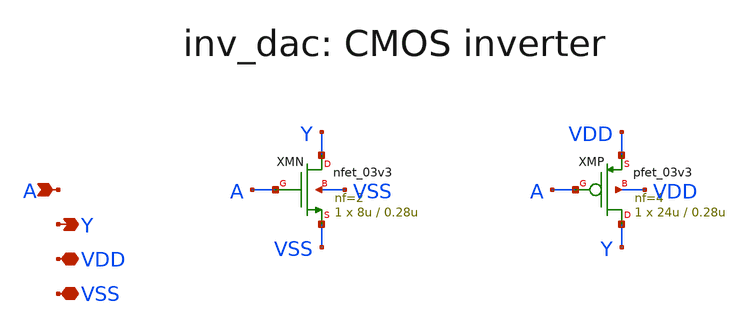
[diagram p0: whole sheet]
** sch_path: v1_claude/xschem/inv_dac.sch
**.subckt inv_dac A Y VDD VSS
*.ipin A
*.opin Y
*.iopin VDD
*.iopin VSS
XMN Y A VSS VSS nfet_03v3 L=0.28u W=8u nf=2 ad='int((nf+1)/2) * W/nf * 0.18u' as='int((nf+2)/2) * W/nf * 0.18u'
+ pd='2*int((nf+1)/2) * (W/nf + 0.18u)' ps='2*int((nf+2)/2) * (W/nf + 0.18u)' nrd='0.18u / W' nrs='0.18u / W'
+ sa=0 sb=0 sd=0 m=1
XMP Y A VDD VDD pfet_03v3 L=0.28u W=24u nf=4 ad='int((nf+1)/2) * W/nf * 0.18u' as='int((nf+2)/2) * W/nf * 0.18u'
+ pd='2*int((nf+1)/2) * (W/nf + 0.18u)' ps='2*int((nf+2)/2) * (W/nf + 0.18u)' nrd='0.18u / W' nrs='0.18u / W'
+ sa=0 sb=0 sd=0 m=1
**.ends
.end
